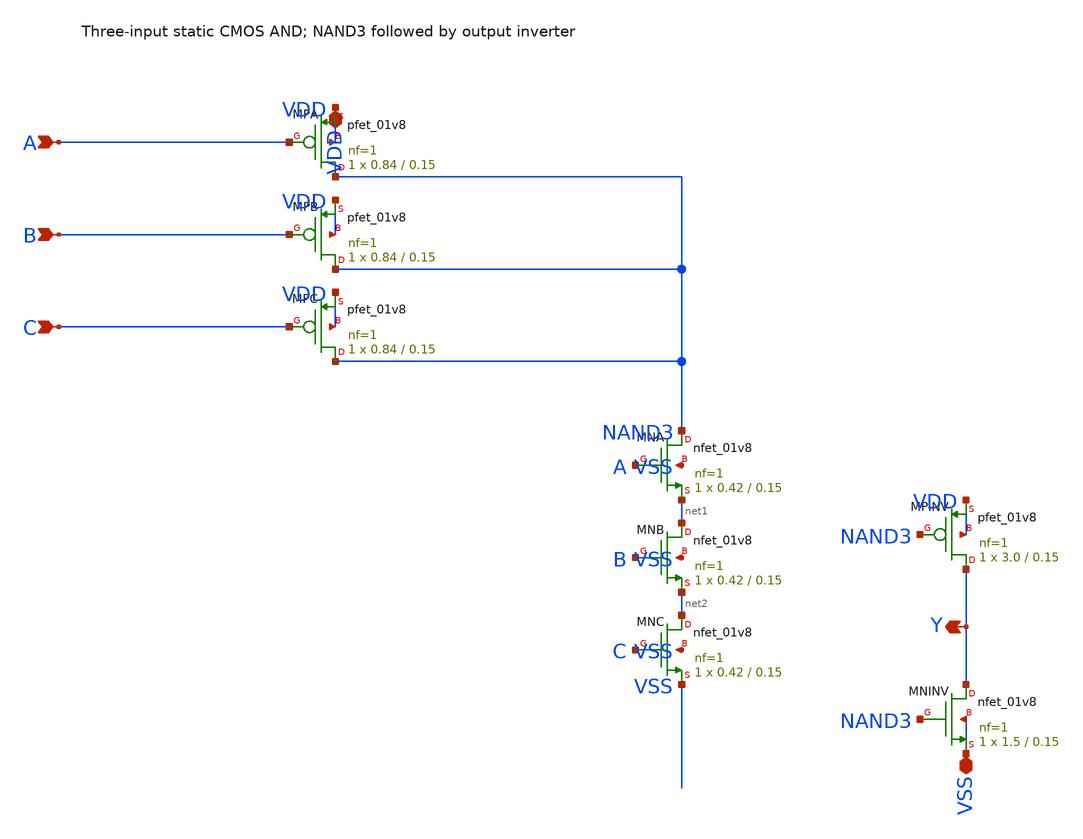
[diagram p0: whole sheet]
** sch_path: cells/control/phase_and3.sch
**.subckt phase_and3 VDD A B C Y VSS
*.iopin VDD
*.ipin A
*.ipin B
*.ipin C
*.opin Y
*.iopin VSS
XMPA NAND3 A VDD VDD sky130_fd_pr__pfet_01v8 L=0.15 W=0.84 nf=1 ad='int((nf+1)/2) * W/nf * 0.29' as='int((nf+2)/2) * W/nf * 0.29'
+ pd='2*int((nf+1)/2) * (W/nf + 0.29)' ps='2*int((nf+2)/2) * (W/nf + 0.29)' nrd='0.29 / W' nrs='0.29 / W'
+ sa=0 sb=0 sd=0 mult=1 m=1
XMPB NAND3 B VDD VDD sky130_fd_pr__pfet_01v8 L=0.15 W=0.84 nf=1 ad='int((nf+1)/2) * W/nf * 0.29' as='int((nf+2)/2) * W/nf * 0.29'
+ pd='2*int((nf+1)/2) * (W/nf + 0.29)' ps='2*int((nf+2)/2) * (W/nf + 0.29)' nrd='0.29 / W' nrs='0.29 / W'
+ sa=0 sb=0 sd=0 mult=1 m=1
XMPC NAND3 C VDD VDD sky130_fd_pr__pfet_01v8 L=0.15 W=0.84 nf=1 ad='int((nf+1)/2) * W/nf * 0.29' as='int((nf+2)/2) * W/nf * 0.29'
+ pd='2*int((nf+1)/2) * (W/nf + 0.29)' ps='2*int((nf+2)/2) * (W/nf + 0.29)' nrd='0.29 / W' nrs='0.29 / W'
+ sa=0 sb=0 sd=0 mult=1 m=1
XMNA NAND3 A net1 VSS sky130_fd_pr__nfet_01v8 L=0.15 W=0.42 nf=1 ad='int((1 + 1)/2) * 0.42 / 1 * 0.29'
+ as='int((1 + 2)/2) * 0.42 / 1 * 0.29' pd='2*int((1 + 1)/2) * (0.42 / 1 + 0.29)' ps='2*int((1 + 2)/2) * (0.42 / 1 + 0.29)'
+ nrd='0.29 / 0.42 ' nrs='0.29 / 0.42 ' sa=0 sb=0 sd=0 mult=1 m=1
XMNB net1 B net2 VSS sky130_fd_pr__nfet_01v8 L=0.15 W=0.42 nf=1 ad='int((1 + 1)/2) * 0.42 / 1 * 0.29'
+ as='int((1 + 2)/2) * 0.42 / 1 * 0.29' pd='2*int((1 + 1)/2) * (0.42 / 1 + 0.29)' ps='2*int((1 + 2)/2) * (0.42 / 1 + 0.29)'
+ nrd='0.29 / 0.42 ' nrs='0.29 / 0.42 ' sa=0 sb=0 sd=0 mult=1 m=1
XMNC net2 C VSS VSS sky130_fd_pr__nfet_01v8 L=0.15 W=0.42 nf=1 ad='int((1 + 1)/2) * 0.42 / 1 * 0.29'
+ as='int((1 + 2)/2) * 0.42 / 1 * 0.29' pd='2*int((1 + 1)/2) * (0.42 / 1 + 0.29)' ps='2*int((1 + 2)/2) * (0.42 / 1 + 0.29)'
+ nrd='0.29 / 0.42 ' nrs='0.29 / 0.42 ' sa=0 sb=0 sd=0 mult=1 m=1
XMPINV Y NAND3 VDD VDD sky130_fd_pr__pfet_01v8 L=0.15 W=3.0 nf=1 ad='int((nf+1)/2) * W/nf * 0.29' as='int((nf+2)/2) * W/nf * 0.29'
+ pd='2*int((nf+1)/2) * (W/nf + 0.29)' ps='2*int((nf+2)/2) * (W/nf + 0.29)' nrd='0.29 / W' nrs='0.29 / W'
+ sa=0 sb=0 sd=0 mult=1 m=1
XMNINV Y NAND3 VSS VSS sky130_fd_pr__nfet_01v8 L=0.15 W=1.5 nf=1 ad='int((1 + 1)/2) * 1.5 / 1 * 0.29'
+ as='int((1 + 2)/2) * 1.5 / 1 * 0.29' pd='2*int((1 + 1)/2) * (1.5 / 1 + 0.29)' ps='2*int((1 + 2)/2) * (1.5 / 1 + 0.29)'
+ nrd='0.29 / 1.5 ' nrs='0.29 / 1.5 ' sa=0 sb=0 sd=0 mult=1 m=1
**.ends
.end
